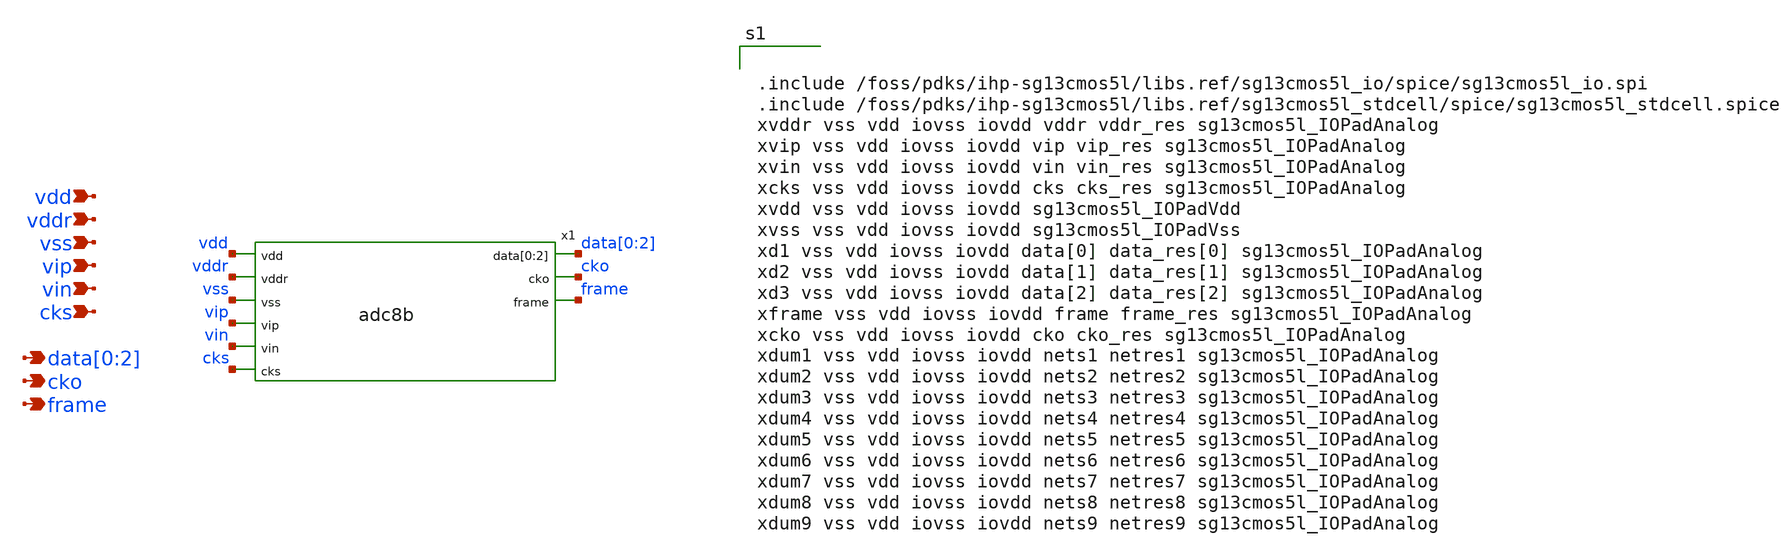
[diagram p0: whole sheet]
** sch_path: MSPHY9932-main/schematic/xschem/MSPHY9932.sch
**.subckt MSPHY9932 vdd vddr vss vip vin cks data[0],data[1],data[2] cko frame
*.ipin vdd
*.ipin vddr
*.ipin vss
*.ipin vip
*.ipin vin
*.ipin cks
*.opin data[0],data[1],data[2]
*.opin cko
*.opin frame
x1 vdd vddr vss vip vin cks data[0] data[1] data[2] cko frame adc8b
**** begin user architecture code


.include /foss/pdks/ihp-sg13cmos5l/libs.ref/sg13cmos5l_io/spice/sg13cmos5l_io.spi
.include /foss/pdks/ihp-sg13cmos5l/libs.ref/sg13cmos5l_stdcell/spice/sg13cmos5l_stdcell.spice
xvddr vss vdd iovss iovdd vddr vddr_res sg13cmos5l_IOPadAnalog
xvip vss vdd iovss iovdd vip vip_res sg13cmos5l_IOPadAnalog
xvin vss vdd iovss iovdd vin vin_res sg13cmos5l_IOPadAnalog
xcks vss vdd iovss iovdd cks cks_res sg13cmos5l_IOPadAnalog
xvdd vss vdd iovss iovdd sg13cmos5l_IOPadVdd
xvss vss vdd iovss iovdd sg13cmos5l_IOPadVss
xd1 vss vdd iovss iovdd data[0] data_res[0] sg13cmos5l_IOPadAnalog
xd2 vss vdd iovss iovdd data[1] data_res[1] sg13cmos5l_IOPadAnalog
xd3 vss vdd iovss iovdd data[2] data_res[2] sg13cmos5l_IOPadAnalog
xframe vss vdd iovss iovdd frame frame_res sg13cmos5l_IOPadAnalog
xcko vss vdd iovss iovdd cko cko_res sg13cmos5l_IOPadAnalog
xdum1 vss vdd iovss iovdd nets1 netres1 sg13cmos5l_IOPadAnalog
xdum2 vss vdd iovss iovdd nets2 netres2 sg13cmos5l_IOPadAnalog
xdum3 vss vdd iovss iovdd nets3 netres3 sg13cmos5l_IOPadAnalog
xdum4 vss vdd iovss iovdd nets4 netres4 sg13cmos5l_IOPadAnalog
xdum5 vss vdd iovss iovdd nets5 netres5 sg13cmos5l_IOPadAnalog
xdum6 vss vdd iovss iovdd nets6 netres6 sg13cmos5l_IOPadAnalog
xdum7 vss vdd iovss iovdd nets7 netres7 sg13cmos5l_IOPadAnalog
xdum8 vss vdd iovss iovdd nets8 netres8 sg13cmos5l_IOPadAnalog
xdum9 vss vdd iovss iovdd nets9 netres9 sg13cmos5l_IOPadAnalog


**** end user architecture code
**.ends
.end
